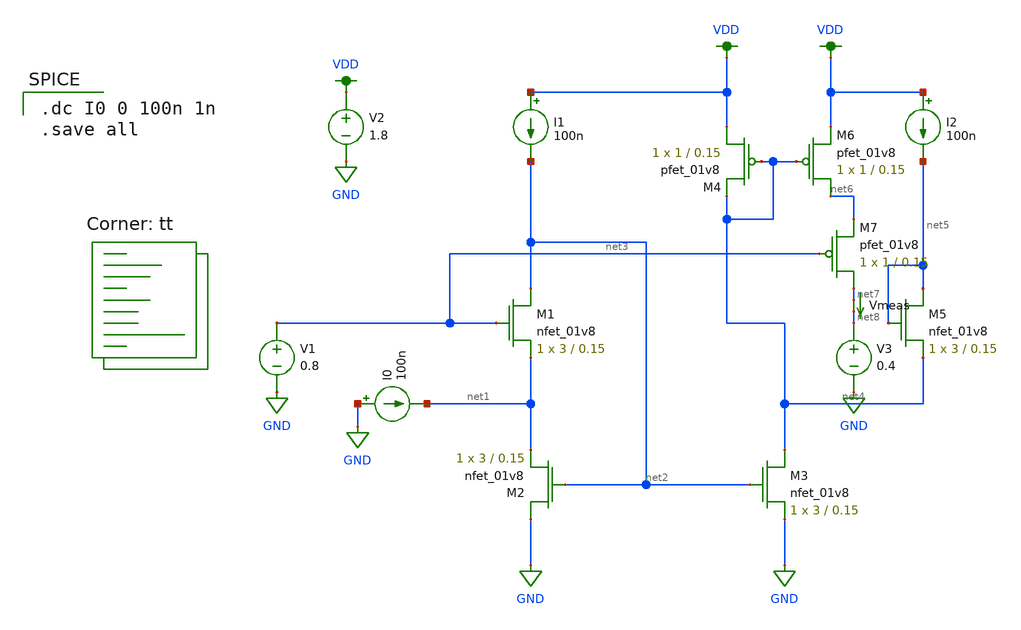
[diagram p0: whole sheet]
** sch_path: test_fvfccm.sch
**.subckt test_fvfccm
XM1 net2 net3 net1 GND sky130_fd_pr__nfet_01v8 L=0.15 W=3 nf=1 ad='int((nf+1)/2) * W/nf * 0.29' as='int((nf+2)/2) * W/nf * 0.29'
+ pd='2*int((nf+1)/2) * (W/nf + 0.29)' ps='2*int((nf+2)/2) * (W/nf + 0.29)' nrd='0.29 / W' nrs='0.29 / W'
+ sa=0 sb=0 sd=0 mult=1 m=1
XM2 GND net2 net1 GND sky130_fd_pr__nfet_01v8 L=0.15 W=3 nf=1 ad='int((nf+1)/2) * W/nf * 0.29' as='int((nf+2)/2) * W/nf * 0.29'
+ pd='2*int((nf+1)/2) * (W/nf + 0.29)' ps='2*int((nf+2)/2) * (W/nf + 0.29)' nrd='0.29 / W' nrs='0.29 / W'
+ sa=0 sb=0 sd=0 mult=1 m=1
I0 GND net1 100n
V1 net3 GND 0.8
I1 VDD net2 100n
V2 VDD GND 1.8
XM3 net4 net2 GND GND sky130_fd_pr__nfet_01v8 L=0.15 W=3 nf=1 ad='int((nf+1)/2) * W/nf * 0.29' as='int((nf+2)/2) * W/nf * 0.29'
+ pd='2*int((nf+1)/2) * (W/nf + 0.29)' ps='2*int((nf+2)/2) * (W/nf + 0.29)' nrd='0.29 / W' nrs='0.29 / W'
+ sa=0 sb=0 sd=0 mult=1 m=1
XM5 net5 net5 net4 GND sky130_fd_pr__nfet_01v8 L=0.15 W=3 nf=1 ad='int((nf+1)/2) * W/nf * 0.29' as='int((nf+2)/2) * W/nf * 0.29'
+ pd='2*int((nf+1)/2) * (W/nf + 0.29)' ps='2*int((nf+2)/2) * (W/nf + 0.29)' nrd='0.29 / W' nrs='0.29 / W'
+ sa=0 sb=0 sd=0 mult=1 m=1
I2 VDD net5 100n
Vmeas net7 net8 0
.save i(vmeas)
XM4 VDD net4 net4 VDD sky130_fd_pr__pfet_01v8 L=0.15 W=1 nf=1 ad='int((nf+1)/2) * W/nf * 0.29' as='int((nf+2)/2) * W/nf * 0.29'
+ pd='2*int((nf+1)/2) * (W/nf + 0.29)' ps='2*int((nf+2)/2) * (W/nf + 0.29)' nrd='0.29 / W' nrs='0.29 / W'
+ sa=0 sb=0 sd=0 mult=1 m=1
XM6 net6 net4 VDD VDD sky130_fd_pr__pfet_01v8 L=0.15 W=1 nf=1 ad='int((nf+1)/2) * W/nf * 0.29' as='int((nf+2)/2) * W/nf * 0.29'
+ pd='2*int((nf+1)/2) * (W/nf + 0.29)' ps='2*int((nf+2)/2) * (W/nf + 0.29)' nrd='0.29 / W' nrs='0.29 / W'
+ sa=0 sb=0 sd=0 mult=1 m=1
XM7 net7 net3 net6 VDD sky130_fd_pr__pfet_01v8 L=0.15 W=1 nf=1 ad='int((nf+1)/2) * W/nf * 0.29' as='int((nf+2)/2) * W/nf * 0.29'
+ pd='2*int((nf+1)/2) * (W/nf + 0.29)' ps='2*int((nf+2)/2) * (W/nf + 0.29)' nrd='0.29 / W' nrs='0.29 / W'
+ sa=0 sb=0 sd=0 mult=1 m=1
V3 net8 GND 0.4
**** begin user architecture code

.dc I0 0 100n 1n
.save all

.lib $::SKYWATER_MODELS/sky130.lib.spice tt
**** end user architecture code
**.ends
.GLOBAL GND
.GLOBAL VDD
.end
